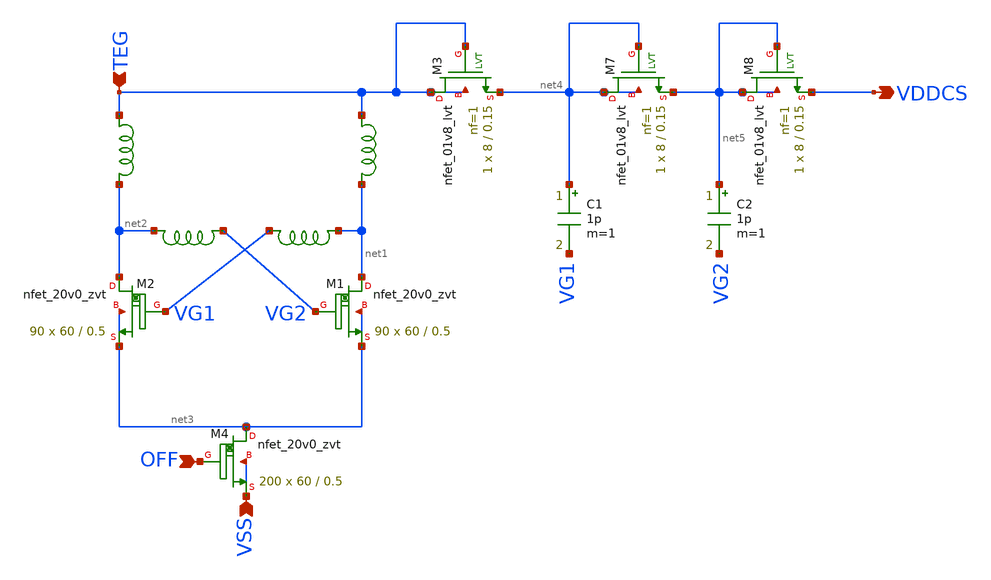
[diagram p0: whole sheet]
** sch_path: design/LELO_SVOD_SKY130A/LELO_COLD_START.sch
**.subckt LELO_COLD_START VSS TEG VDDCS OFF
*.ipin VSS
*.ipin TEG
*.opin VDDCS
*.ipin OFF
XM1 net1 VG2 net3 net3 sky130_fd_pr__nfet_20v0_zvt W=60 L=0.5 m=90
XM2 net2 VG1 net3 net3 sky130_fd_pr__nfet_20v0_zvt W=60 L=0.5 m=90
XM3 TEG TEG net4 TEG sky130_fd_pr__nfet_01v8_lvt L=0.15 W=8 nf=1 ad='int((1 + 1)/2) * 8 / 1 * 0.29' as='int((1 + 2)/2) * 8 / 1 * 0.29'
+ pd='2*int((1 + 1)/2) * (8 / 1 + 0.29)' ps='2*int((1 + 2)/2) * (8 / 1 + 0.29)' nrd='0.29 / 8 ' nrs='0.29 / 8 '
+ sa=0 sb=0 sd=0 mult=1 m=1
XM7 net4 net4 net5 net4 sky130_fd_pr__nfet_01v8_lvt L=0.15 W=8 nf=1 ad='int((1 + 1)/2) * 8 / 1 * 0.29'
+ as='int((1 + 2)/2) * 8 / 1 * 0.29' pd='2*int((1 + 1)/2) * (8 / 1 + 0.29)' ps='2*int((1 + 2)/2) * (8 / 1 + 0.29)'
+ nrd='0.29 / 8 ' nrs='0.29 / 8 ' sa=0 sb=0 sd=0 mult=1 m=1
XM8 net5 net5 VDDCS net5 sky130_fd_pr__nfet_01v8_lvt L=0.15 W=8 nf=1 ad='int((1 + 1)/2) * 8 / 1 * 0.29'
+ as='int((1 + 2)/2) * 8 / 1 * 0.29' pd='2*int((1 + 1)/2) * (8 / 1 + 0.29)' ps='2*int((1 + 2)/2) * (8 / 1 + 0.29)'
+ nrd='0.29 / 8 ' nrs='0.29 / 8 ' sa=0 sb=0 sd=0 mult=1 m=1
XM4 net3 OFF VSS VSS sky130_fd_pr__nfet_20v0_zvt W=60 L=0.5 m=200
x3 net1 VG1 1812PS-474_imp
x4 VG2 net2 1812PS-474_imp
x1 TEG net1 1812PS-562_imp
x2 TEG net2 1812PS-562_imp
C1 net4 VG1 1p m=1
C2 net5 VG2 1p m=1
**.ends

* expanding   symbol:  LELO_SVOD_SKY130A/1812PS-474_imp.sym # of pins=2
** sym_path: design/LELO_SVOD_SKY130A/1812PS-474_imp.sym

.subckt 1812PS-474_imp port1 port2
X1 port1 port2 Model1D R1=105 R2=5.9 C= 3.15p K1=1E-06 K2=108.9 K3= 470u K4=0.000001 K5=0.000001 L=0
+ Is=0 a=0 L_Z0=0 L_EL=0 L_F0=0E6 PkZ=191622.479
.ends 1812PS-474_imp

* expanding   symbol:  LELO_SVOD_SKY130A/1812PS-562_imp.sym # of pins=2
** sym_path: design/LELO_SVOD_SKY130A/1812PS-562_imp.sym

.subckt 1812PS-562_imp port1 port2
X1 port1 port2 Model1D R1=22 R2=0.12 C= 0.289p K1=0.000001 K2=0.494 K3= 5.6u K4=0.00145 K5=0.0000514
+ L=0 Is=0 a=0 L_Z0=0 L_EL=0 L_F0=0E6 PkZ=5489.2717
.ends 1812PS-562_imp
.end
